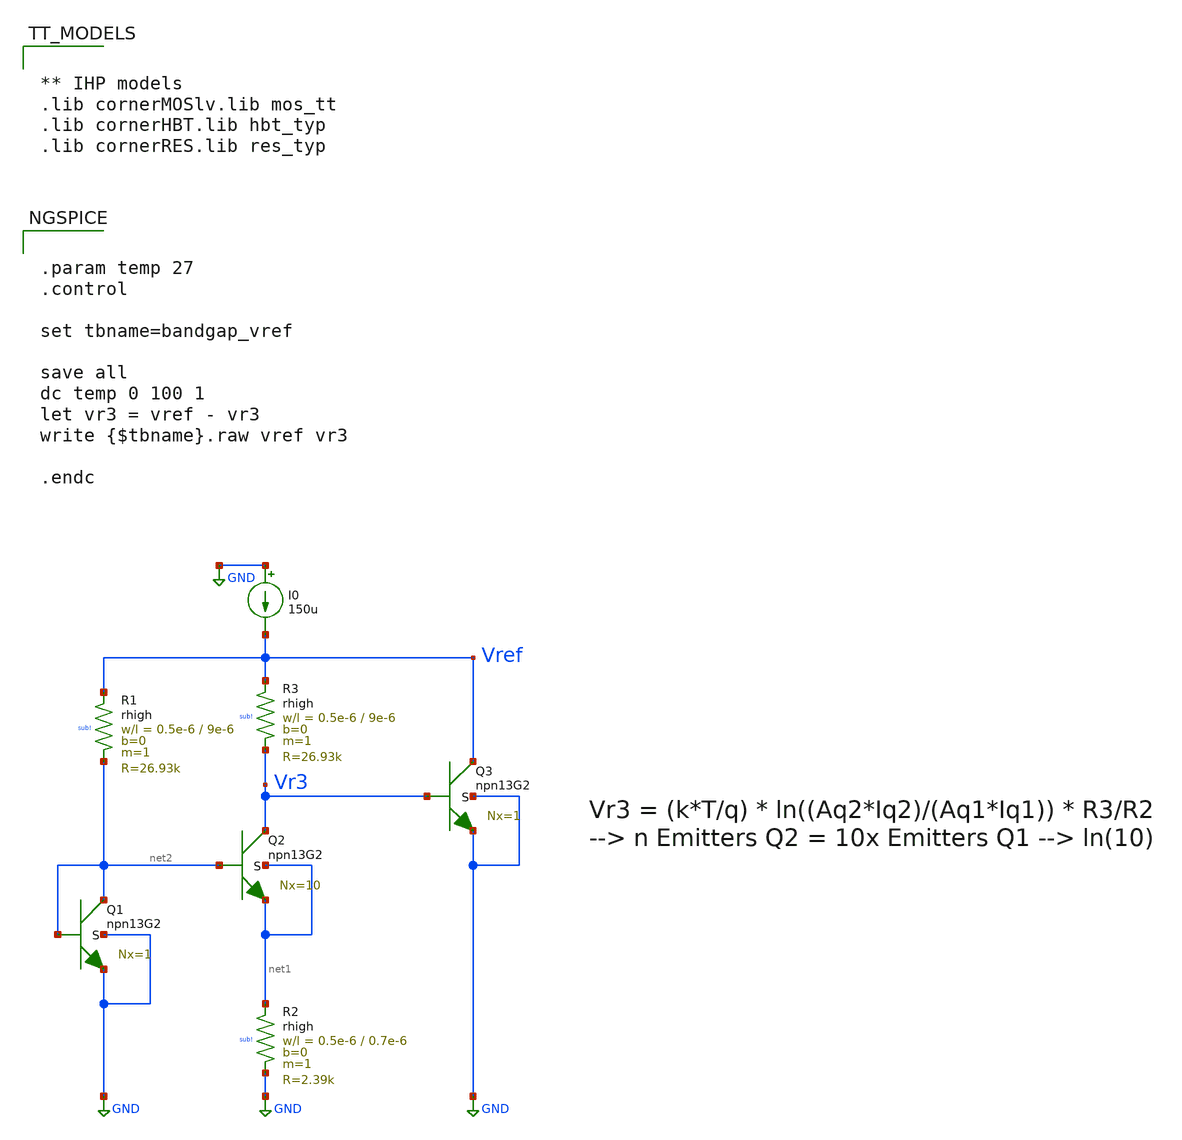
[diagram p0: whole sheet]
** sch_path: TempSensor/design_data/xschem/band_gap_vref.sch
**.subckt band_gap_vref
XQ1 net2 net2 GND GND npn13G2 Nx=1 mm_ok=1
XQ2 Vr3 net2 net1 net1 npn13G2 Nx=10 mm_ok=1
XQ3 Vref Vr3 GND GND npn13G2 Nx=1 mm_ok=1
XR1 Vref net2 sub! rhigh w=0.5e-6 l=9e-6 m=1 b=0 mm_ok=1
XR3 Vref Vr3 sub! rhigh w=0.5e-6 l=9e-6 m=1 b=0 mm_ok=1
XR2 net1 GND sub! rhigh w=0.5e-6 l=0.7e-6 m=1 b=0 mm_ok=1
I0 GND Vref 150u
**** begin user architecture code


.param temp 27
.control

set tbname=bandgap_vref

save all
dc temp 0 100 1
let vr3 = vref - vr3
write {$tbname}.raw vref vr3

.endc




** IHP models
.lib cornerMOSlv.lib mos_tt
.lib cornerHBT.lib hbt_typ
.lib cornerRES.lib res_typ


**** end user architecture code
**.ends
.GLOBAL GND
.end
